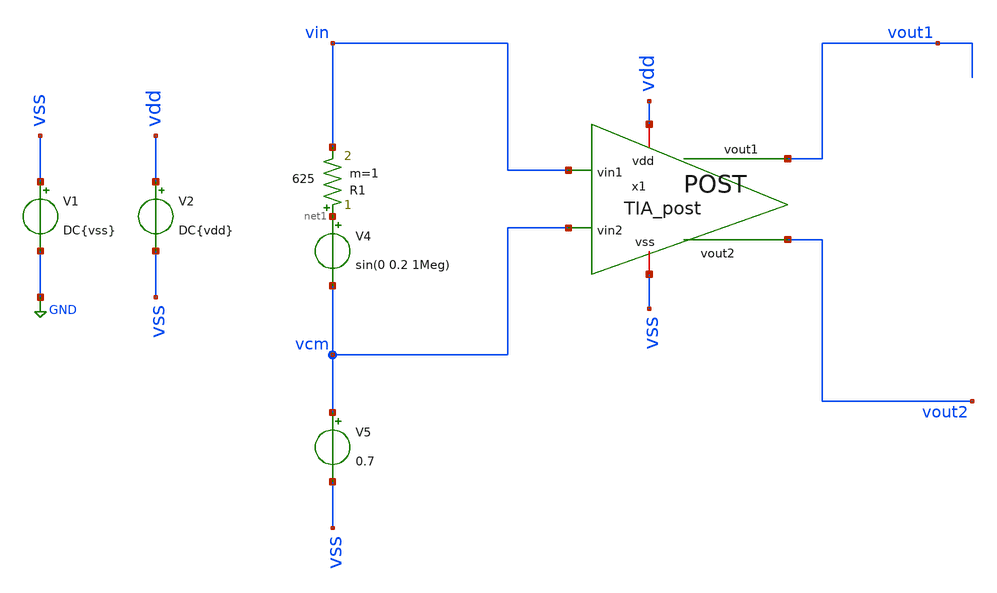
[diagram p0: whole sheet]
** sch_path: full/tb_Full.sch
**.subckt tb_Full
V1 vss GND DC{vss}
V2 vdd vss DC{vdd}
V4 net1 vcm sin(0 0.2 1Meg)
V5 vcm vss 0.7
R1 net1 vin 625 m=1
x1 vin vcm vout1 vout2 vdd vss TIA_post
**** begin user architecture code




* Circuit Parameters
.param iref = 100u
.param vdd  = 1.8
.param vss  = 0.0
.options TEMP = 65.0

* Include Models
.inc /home/alex/Desktop/EDA/TIA_IPN/sch/TIA_post.spice

* OP Parameters & Singals to save
.save all

*Simulations
.control

  reset
  tran 0.01u 11u
  setplot tran1
  plot v(vin) v(vcm) v(vout1) v(vout2)
  plot i(v4)

  write tb_tia_post.raw




.endc

.end



** opencircuitdesign pdks install
.lib $::SKYWATER_MODELS/sky130.lib.spice tt


**** end user architecture code
**.ends
.GLOBAL GND
.end
